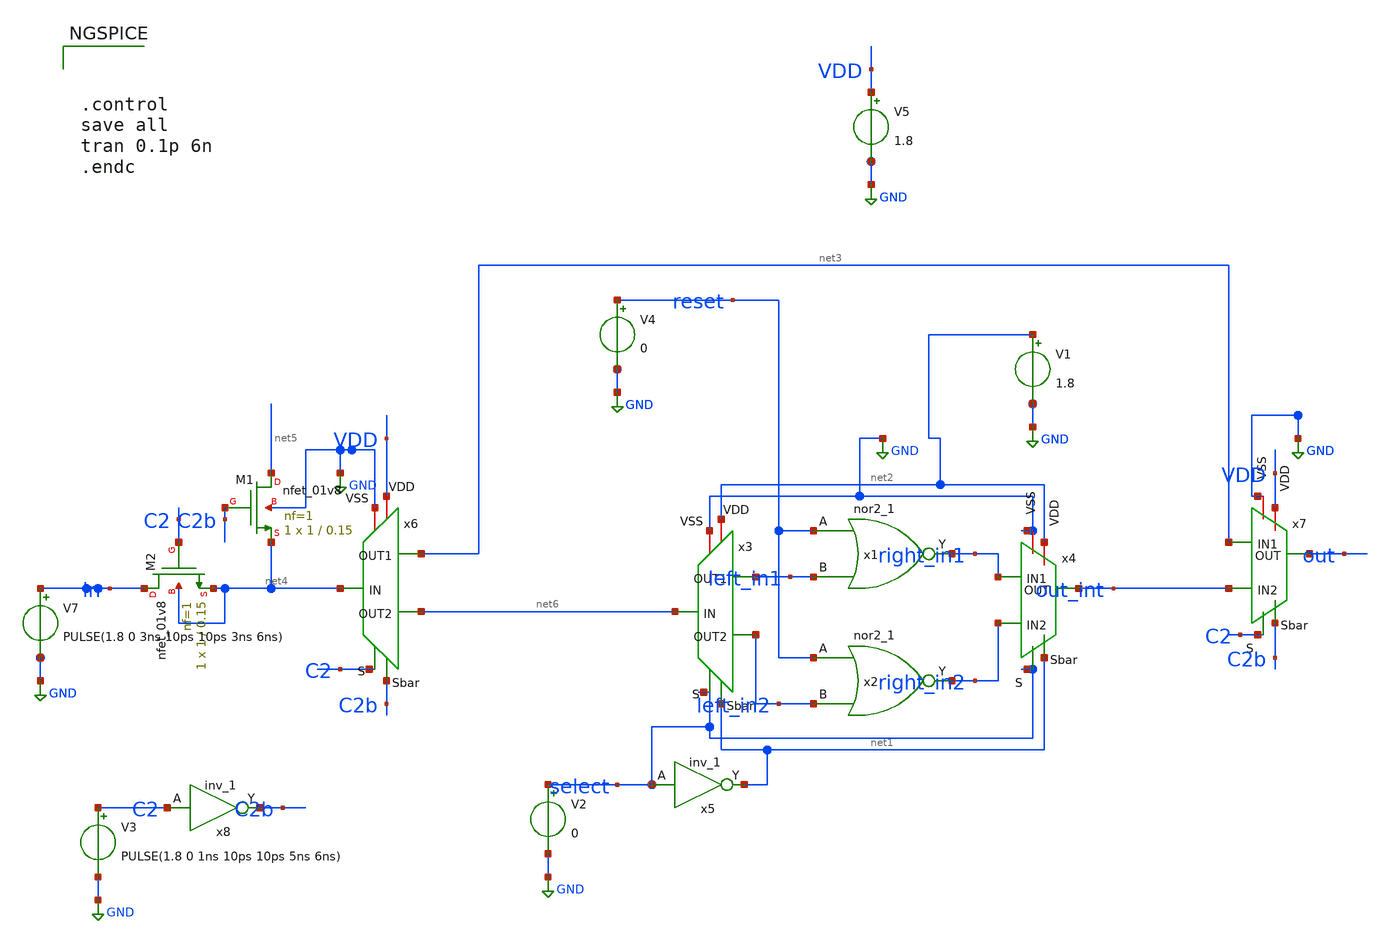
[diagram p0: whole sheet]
** sch_path: xiaolin/singlestage_wtc_tb.sch
**.subckt singlestage_wtc_tb
x1 reset left_in1 GND GND VDD VDD right_in1 sky130_fd_sc_hd__nor2_1
x2 reset left_in2 GND GND VDD VDD right_in2 sky130_fd_sc_hd__nor2_1
x3 select GND left_in1 net2 net6 net1 left_in2 demux2-1
x4 select GND right_in1 net2 out_int net1 right_in2 mux2-1
x5 select GND GND VDD VDD net1 sky130_fd_sc_hd__inv_1
V1 net2 GND 1.8
V2 select GND 0
V4 reset GND 0
V5 VDD GND 1.8
x6 C2 GND net3 VDD net4 C2b net6 demux2-1
XM1 net5 C2b net4 GND sky130_fd_pr__nfet_01v8 L=0.15 W=1 nf=1 ad='int((nf+1)/2) * W/nf * 0.29' as='int((nf+2)/2) * W/nf * 0.29'
+ pd='2*int((nf+1)/2) * (W/nf + 0.29)' ps='2*int((nf+2)/2) * (W/nf + 0.29)' nrd='0.29 / W' nrs='0.29 / W'
+ sa=0 sb=0 sd=0 mult=1 m=1
XM2 in C2 net4 net4 sky130_fd_pr__nfet_01v8 L=0.15 W=1 nf=1 ad='int((nf+1)/2) * W/nf * 0.29' as='int((nf+2)/2) * W/nf * 0.29'
+ pd='2*int((nf+1)/2) * (W/nf + 0.29)' ps='2*int((nf+2)/2) * (W/nf + 0.29)' nrd='0.29 / W' nrs='0.29 / W'
+ sa=0 sb=0 sd=0 mult=1 m=1
x7 C2 GND net3 VDD out C2b out_int mux2-1
x8 C2 GND GND VDD VDD C2b sky130_fd_sc_hd__inv_1
V7 in GND PULSE(1.8 0 3ns 10ps 10ps 3ns 6ns)
V3 C2 GND PULSE(1.8 0 1ns 10ps 10ps 5ns 6ns)
**** begin user architecture code

** opencircuitdesign pdks install
*.lib /farmshare/home/classes/ee/372/PDKs/open_pdks/sky130/sky130A/libs.tech/ngspice/sky130.lib.spice tt
.lib ~/372puf/ee372/sky130A/libs.tech/ngspice/sky130.lib.spice tt
.include /farmshare/home/classes/ee/372/PDKs/open_pdks/sky130/sky130A/libs.ref/sky130_fd_sc_hd/spice/sky130_fd_sc_hd.spice






.control
save all
tran 0.1p 6n
.endc


**** end user architecture code
**.ends

* expanding   symbol:  demux2-1.sym # of pins=7
** sym_path: xiaolin/demux2-1.sym
** sch_path: xiaolin/demux2-1.sch
.subckt demux2-1 S VSS OUT1 VDD IN Sbar OUT2
*.ipin Sbar
*.ipin S
*.iopin VSS
*.iopin VDD
*.opin OUT1
*.opin OUT2
*.ipin IN
XM2 IN S OUT1 VSS sky130_fd_pr__nfet_01v8 L=0.15 W=0.65 nf=1 ad='int((nf+1)/2) * W/nf * 0.29' as='int((nf+2)/2) * W/nf * 0.29'
+ pd='2*int((nf+1)/2) * (W/nf + 0.29)' ps='2*int((nf+2)/2) * (W/nf + 0.29)' nrd='0.29 / W' nrs='0.29 / W'
+ sa=0 sb=0 sd=0 mult=1 m=1
XM1 IN Sbar OUT2 VSS sky130_fd_pr__nfet_01v8 L=0.15 W=0.65 nf=1 ad='int((nf+1)/2) * W/nf * 0.29' as='int((nf+2)/2) * W/nf * 0.29'
+ pd='2*int((nf+1)/2) * (W/nf + 0.29)' ps='2*int((nf+2)/2) * (W/nf + 0.29)' nrd='0.29 / W' nrs='0.29 / W'
+ sa=0 sb=0 sd=0 mult=1 m=1
XM3 IN S OUT2 VDD sky130_fd_pr__pfet_01v8_hvt L=0.15 W=1 nf=1 ad='int((nf+1)/2) * W/nf * 0.29' as='int((nf+2)/2) * W/nf * 0.29'
+ pd='2*int((nf+1)/2) * (W/nf + 0.29)' ps='2*int((nf+2)/2) * (W/nf + 0.29)' nrd='0.29 / W' nrs='0.29 / W'
+ sa=0 sb=0 sd=0 mult=1 m=1
XM4 IN Sbar OUT1 VDD sky130_fd_pr__pfet_01v8_hvt L=0.15 W=1 nf=1 ad='int((nf+1)/2) * W/nf * 0.29' as='int((nf+2)/2) * W/nf * 0.29'
+ pd='2*int((nf+1)/2) * (W/nf + 0.29)' ps='2*int((nf+2)/2) * (W/nf + 0.29)' nrd='0.29 / W' nrs='0.29 / W'
+ sa=0 sb=0 sd=0 mult=1 m=1
XM5 IN S OUT2 VDD sky130_fd_pr__pfet_01v8_hvt L=0.15 W=1 nf=1 ad='int((nf+1)/2) * W/nf * 0.29' as='int((nf+2)/2) * W/nf * 0.29'
+ pd='2*int((nf+1)/2) * (W/nf + 0.29)' ps='2*int((nf+2)/2) * (W/nf + 0.29)' nrd='0.29 / W' nrs='0.29 / W'
+ sa=0 sb=0 sd=0 mult=1 m=1
.ends


* expanding   symbol:  mux2-1.sym # of pins=7
** sym_path: design/mux2-1.sym
** sch_path: design/mux2-1.sch
.subckt mux2-1 S VSS IN1 VDD OUT Sbar IN2
*.ipin IN1
*.ipin IN2
*.ipin Sbar
*.ipin S
*.opin OUT
*.iopin VSS
*.iopin VDD
XM2 IN1 S OUT VSS sky130_fd_pr__nfet_01v8 L=0.15 W=0.65 nf=1 ad='int((nf+1)/2) * W/nf * 0.29' as='int((nf+2)/2) * W/nf * 0.29'
+ pd='2*int((nf+1)/2) * (W/nf + 0.29)' ps='2*int((nf+2)/2) * (W/nf + 0.29)' nrd='0.29 / W' nrs='0.29 / W'
+ sa=0 sb=0 sd=0 mult=1 m=1
XM1 IN2 Sbar OUT VSS sky130_fd_pr__nfet_01v8 L=0.15 W=0.65 nf=1 ad='int((nf+1)/2) * W/nf * 0.29' as='int((nf+2)/2) * W/nf * 0.29'
+ pd='2*int((nf+1)/2) * (W/nf + 0.29)' ps='2*int((nf+2)/2) * (W/nf + 0.29)' nrd='0.29 / W' nrs='0.29 / W'
+ sa=0 sb=0 sd=0 mult=1 m=1
XM4 IN1 Sbar OUT VDD sky130_fd_pr__pfet_01v8_hvt L=0.15 W=1 nf=1 ad='int((nf+1)/2) * W/nf * 0.29' as='int((nf+2)/2) * W/nf * 0.29'
+ pd='2*int((nf+1)/2) * (W/nf + 0.29)' ps='2*int((nf+2)/2) * (W/nf + 0.29)' nrd='0.29 / W' nrs='0.29 / W'
+ sa=0 sb=0 sd=0 mult=1 m=1
XM5 IN2 S OUT VDD sky130_fd_pr__pfet_01v8_hvt L=0.15 W=1 nf=1 ad='int((nf+1)/2) * W/nf * 0.29' as='int((nf+2)/2) * W/nf * 0.29'
+ pd='2*int((nf+1)/2) * (W/nf + 0.29)' ps='2*int((nf+2)/2) * (W/nf + 0.29)' nrd='0.29 / W' nrs='0.29 / W'
+ sa=0 sb=0 sd=0 mult=1 m=1
.ends

.GLOBAL GND
.end
